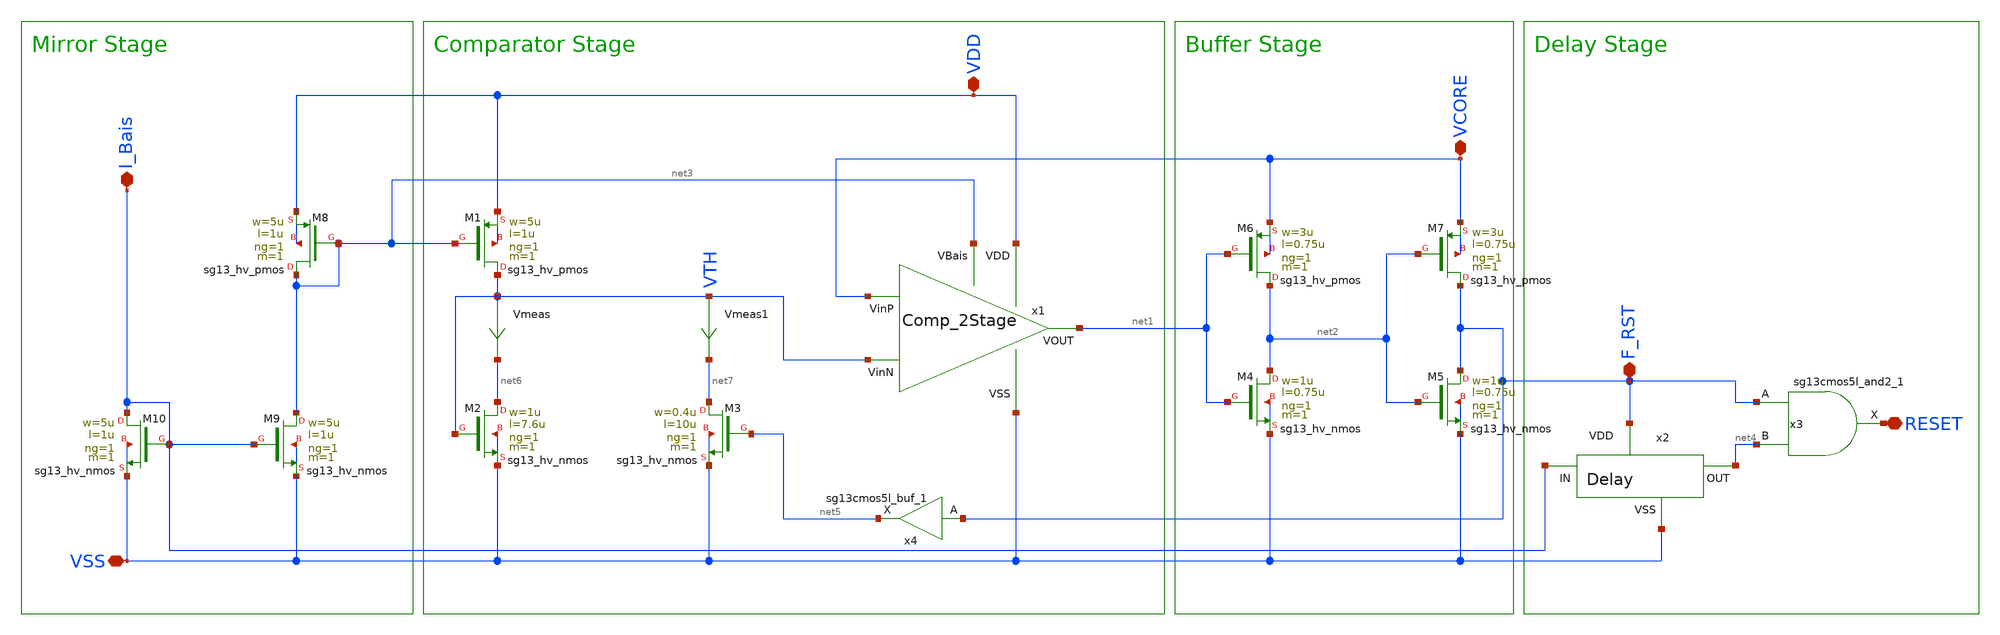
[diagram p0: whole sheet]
** sch_path: LPVSV_Circuit/LPVSV.sch
**.subckt LPVSV VDD VCORE RESET VSS F_RST I_Bais
*.iopin VDD
*.iopin VCORE
*.iopin RESET
*.iopin VSS
*.iopin F_RST
*.iopin I_Bais
XM4 net2 net1 VSS VSS sg13_hv_nmos w=1u l=0.75u ng=1 m=1 mm_ok=1
XM5 F_RST net2 VSS VSS sg13_hv_nmos w=1u l=0.75u ng=1 m=1 mm_ok=1
XM6 net2 net1 VCORE VCORE sg13_hv_pmos w=3u l=0.75u ng=1 m=1 mm_ok=1
XM7 F_RST net2 VCORE VCORE sg13_hv_pmos w=3u l=0.75u ng=1 m=1 mm_ok=1
x2 I_Bais net4 VSS F_RST Delay
x3 RESET F_RST net4 VCORE VSS sg13cmos5l_and2_1
x1 VDD net3 VCORE VTH net1 VSS Comp_2Stage
XM8 net3 net3 VDD VDD sg13_hv_pmos w=5u l=1u ng=1 m=1 mm_ok=1
XM9 net3 I_Bais VSS VSS sg13_hv_nmos w=5u l=1u ng=1 m=1 mm_ok=1
XM10 I_Bais I_Bais VSS VSS sg13_hv_nmos w=5u l=1u ng=1 m=1 mm_ok=1
x4 net5 F_RST VTH VSS sg13cmos5l_buf_1
XM1 VTH net3 VDD VDD sg13_hv_pmos w=5u l=1u ng=1 m=1 mm_ok=1
Vmeas VTH net6 0
.save i(vmeas)
XM2 net6 VTH VSS VSS sg13_hv_nmos w=1u l=7.6u ng=1 m=1 mm_ok=1
XM3 net7 net5 VSS VSS sg13_hv_nmos w=0.4u l=10u ng=1 m=1 mm_ok=1
Vmeas1 VTH net7 0
.save i(vmeas1)
**.ends
.end
